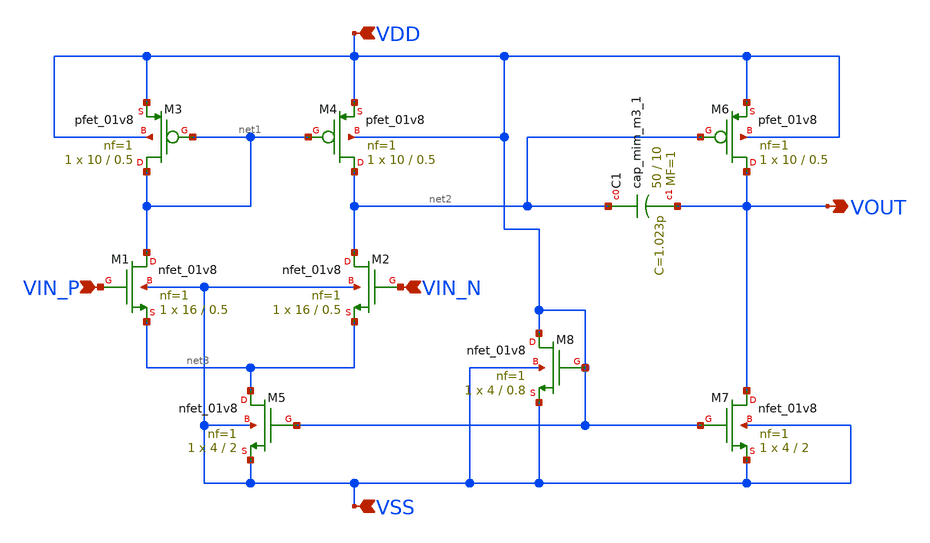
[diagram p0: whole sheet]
** sch_path: analog/schematics/bootcamp_opamp.sch
**.subckt bootcamp_opamp VIN_P VIN_N VDD VSS VOUT
*.ipin VIN_P
*.ipin VIN_N
*.ipin VDD
*.ipin VSS
*.opin VOUT
XM1 net1 VIN_P net3 VSS sky130_fd_pr__nfet_01v8 L=0.5 W=16 nf=1 ad='int((nf+1)/2) * W/nf * 0.29' as='int((nf+2)/2) * W/nf * 0.29'
+ pd='2*int((nf+1)/2) * (W/nf + 0.29)' ps='2*int((nf+2)/2) * (W/nf + 0.29)' nrd='0.29 / W' nrs='0.29 / W'
+ sa=0 sb=0 sd=0 mult=1 m=1
XM2 net2 VIN_N net3 VSS sky130_fd_pr__nfet_01v8 L=0.5 W=16 nf=1 ad='int((nf+1)/2) * W/nf * 0.29' as='int((nf+2)/2) * W/nf * 0.29'
+ pd='2*int((nf+1)/2) * (W/nf + 0.29)' ps='2*int((nf+2)/2) * (W/nf + 0.29)' nrd='0.29 / W' nrs='0.29 / W'
+ sa=0 sb=0 sd=0 mult=1 m=1
XM3 net1 net1 VDD VDD sky130_fd_pr__pfet_01v8 L=0.5 W=10 nf=1 ad='int((nf+1)/2) * W/nf * 0.29' as='int((nf+2)/2) * W/nf * 0.29'
+ pd='2*int((nf+1)/2) * (W/nf + 0.29)' ps='2*int((nf+2)/2) * (W/nf + 0.29)' nrd='0.29 / W' nrs='0.29 / W'
+ sa=0 sb=0 sd=0 mult=1 m=1
XM4 net2 net1 VDD VDD sky130_fd_pr__pfet_01v8 L=0.5 W=10 nf=1 ad='int((nf+1)/2) * W/nf * 0.29' as='int((nf+2)/2) * W/nf * 0.29'
+ pd='2*int((nf+1)/2) * (W/nf + 0.29)' ps='2*int((nf+2)/2) * (W/nf + 0.29)' nrd='0.29 / W' nrs='0.29 / W'
+ sa=0 sb=0 sd=0 mult=1 m=1
XM5 net3 VDD VSS VSS sky130_fd_pr__nfet_01v8 L=2 W=4 nf=1 ad='int((nf+1)/2) * W/nf * 0.29' as='int((nf+2)/2) * W/nf * 0.29'
+ pd='2*int((nf+1)/2) * (W/nf + 0.29)' ps='2*int((nf+2)/2) * (W/nf + 0.29)' nrd='0.29 / W' nrs='0.29 / W'
+ sa=0 sb=0 sd=0 mult=1 m=1
XM6 VOUT net2 VDD VDD sky130_fd_pr__pfet_01v8 L=0.5 W=10 nf=1 ad='int((nf+1)/2) * W/nf * 0.29' as='int((nf+2)/2) * W/nf * 0.29'
+ pd='2*int((nf+1)/2) * (W/nf + 0.29)' ps='2*int((nf+2)/2) * (W/nf + 0.29)' nrd='0.29 / W' nrs='0.29 / W'
+ sa=0 sb=0 sd=0 mult=1 m=1
XM7 VOUT VDD VSS VSS sky130_fd_pr__nfet_01v8 L=2 W=4 nf=1 ad='int((nf+1)/2) * W/nf * 0.29' as='int((nf+2)/2) * W/nf * 0.29'
+ pd='2*int((nf+1)/2) * (W/nf + 0.29)' ps='2*int((nf+2)/2) * (W/nf + 0.29)' nrd='0.29 / W' nrs='0.29 / W'
+ sa=0 sb=0 sd=0 mult=1 m=1
XM8 VDD VDD VSS VSS sky130_fd_pr__nfet_01v8 L=0.8 W=4 nf=1 ad='int((nf+1)/2) * W/nf * 0.29' as='int((nf+2)/2) * W/nf * 0.29'
+ pd='2*int((nf+1)/2) * (W/nf + 0.29)' ps='2*int((nf+2)/2) * (W/nf + 0.29)' nrd='0.29 / W' nrs='0.29 / W'
+ sa=0 sb=0 sd=0 mult=1 m=1
XC1 net2 VOUT sky130_fd_pr__cap_mim_m3_1 W=50 L=10 MF=1 m=1
**.ends
.end
